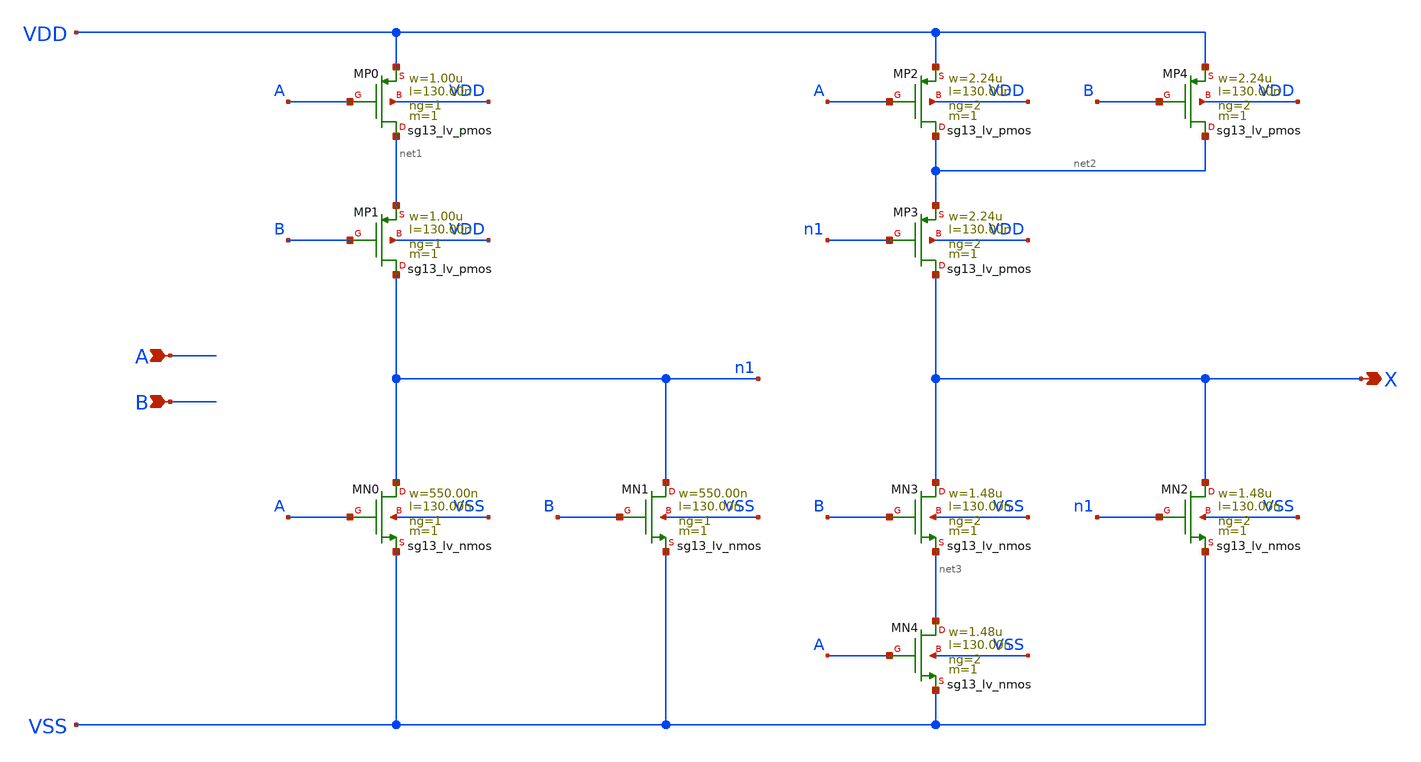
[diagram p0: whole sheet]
** sch_path: outputs/sg13g2_cells/cells/sg13g2_xor2_2/sg13g2_xor2_2.sch
**.subckt sg13g2_xor2_2 A B X
*.ipin A
*.ipin B
*.opin X
XMN0 n1 A VSS VSS sg13_lv_nmos w=550.00n l=130.00n ng=1 m=1 mm_ok=1
XMN3 X B net3 VSS sg13_lv_nmos w=1.48u l=130.00n ng=2 m=1 mm_ok=1
XMN2 X n1 VSS VSS sg13_lv_nmos w=1.48u l=130.00n ng=2 m=1 mm_ok=1
XMN4 net3 A VSS VSS sg13_lv_nmos w=1.48u l=130.00n ng=2 m=1 mm_ok=1
XMN1 n1 B VSS VSS sg13_lv_nmos w=550.00n l=130.00n ng=1 m=1 mm_ok=1
XMP0 net1 A VDD VDD sg13_lv_pmos w=1.00u l=130.00n ng=1 m=1 mm_ok=1
XMP1 n1 B net1 VDD sg13_lv_pmos w=1.00u l=130.00n ng=1 m=1 mm_ok=1
XMP2 net2 A VDD VDD sg13_lv_pmos w=2.24u l=130.00n ng=2 m=1 mm_ok=1
XMP4 net2 B VDD VDD sg13_lv_pmos w=2.24u l=130.00n ng=2 m=1 mm_ok=1
XMP3 X n1 net2 VDD sg13_lv_pmos w=2.24u l=130.00n ng=2 m=1 mm_ok=1
**.ends
.end
